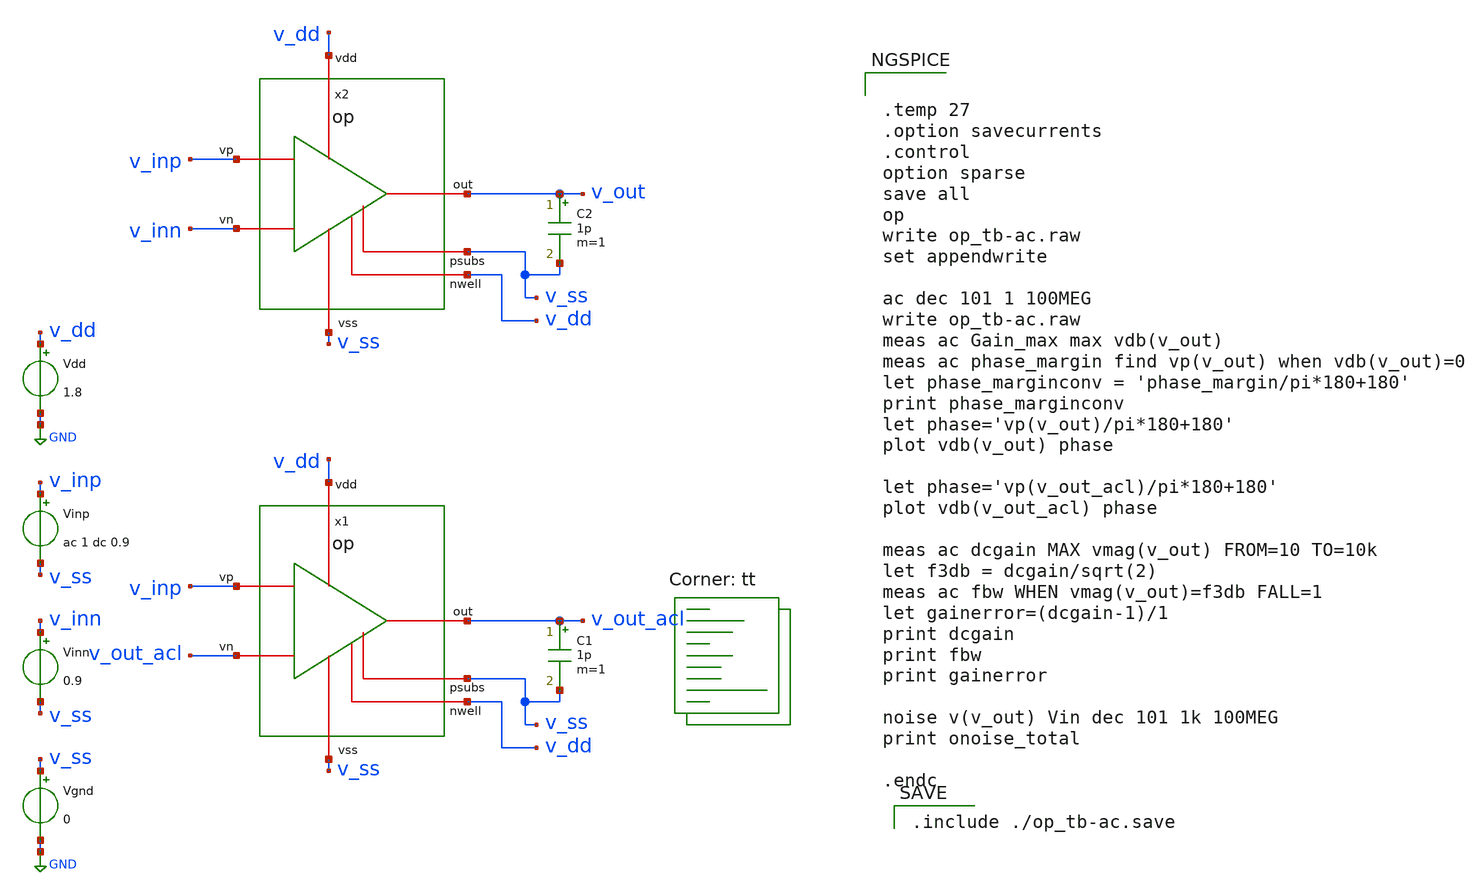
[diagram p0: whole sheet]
** sch_path: xschem/op_tb-ac.sch
**.subckt op_tb-ac
Vdd v_dd GND 1.8
Vinn v_inn v_ss 0.9
x1 v_out_acl v_dd v_ss v_inp v_out_acl v_ss v_dd op
Vgnd v_ss GND 0
C1 v_out_acl v_ss 1p m=1
Vinp v_inp v_ss ac 1 dc 0.9
x2 v_out v_dd v_ss v_inp v_inn v_ss v_dd op
C2 v_out v_ss 1p m=1
**** begin user architecture code
.lib $::SKYWATER_MODELS/sky130.lib.spice tt


.temp 27
.option savecurrents
.control
option sparse
save all
op
write op_tb-ac.raw
set appendwrite

ac dec 101 1 100MEG
write op_tb-ac.raw
meas ac Gain_max max vdb(v_out)
meas ac phase_margin find vp(v_out) when vdb(v_out)=0
let phase_marginconv = 'phase_margin/pi*180+180'
print phase_marginconv
let phase='vp(v_out)/pi*180+180'
plot vdb(v_out) phase

let phase='vp(v_out_acl)/pi*180+180'
plot vdb(v_out_acl) phase

meas ac dcgain MAX vmag(v_out) FROM=10 TO=10k
let f3db = dcgain/sqrt(2)
meas ac fbw WHEN vmag(v_out)=f3db FALL=1
let gainerror=(dcgain-1)/1
print dcgain
print fbw
print gainerror

noise v(v_out) Vin dec 101 1k 100MEG
print onoise_total

.endc


 .include ./op_tb-ac.save

**** end user architecture code
**.ends

* expanding   symbol:  op.sym # of pins=7
** sym_path: xschem/op.sym
** sch_path: xschem/op.sch
.subckt op out vdd vss vp vn psubs nwell
*.iopin vss
*.iopin vdd
*.opin out
*.ipin vp
*.ipin vn
*.iopin psubs
*.iopin nwell
XM3 out net1 vdd nwell sky130_fd_pr__pfet_01v8 L={l3} W={w3} nf={nf3} ad='int((nf+1)/2) * W/nf * 0.29'
+ as='int((nf+2)/2) * W/nf * 0.29' pd='2*int((nf+1)/2) * (W/nf + 0.29)' ps='2*int((nf+2)/2) * (W/nf + 0.29)'
+ nrd='0.29 / W' nrs='0.29 / W' sa=0 sb=0 sd=0 mult=1 m=1
XM1b net1 vn net2 psubs sky130_fd_pr__nfet_01v8 L={l1} W={w1} nf={nf1} ad='int((nf+1)/2) * W/nf * 0.29'
+ as='int((nf+2)/2) * W/nf * 0.29' pd='2*int((nf+1)/2) * (W/nf + 0.29)' ps='2*int((nf+2)/2) * (W/nf + 0.29)'
+ nrd='0.29 / W' nrs='0.29 / W' sa=0 sb=0 sd=0 mult=1 m=1
XM1a net3 vp net2 psubs sky130_fd_pr__nfet_01v8 L={l1} W={w1} nf={nf1} ad='int((nf+1)/2) * W/nf * 0.29'
+ as='int((nf+2)/2) * W/nf * 0.29' pd='2*int((nf+1)/2) * (W/nf + 0.29)' ps='2*int((nf+2)/2) * (W/nf + 0.29)'
+ nrd='0.29 / W' nrs='0.29 / W' sa=0 sb=0 sd=0 mult=1 m=1
XR1 net4 net1 vss sky130_fd_pr__res_high_po_0p35 L={lrz} mult=1 m=1
XC1 out net4 sky130_fd_pr__cap_mim_m3_1 W={wc} L={wc} MF={mc} m={mc}
**** begin user architecture code


.include ../sizing_opamp.spice


**** end user architecture code
XM2a net3 net3 vdd nwell sky130_fd_pr__pfet_01v8 L={l2} W={w2} nf={nf2} ad='int(({nf2} + 1)/2) * {w2} / {nf2} * 0.29'
+ as='int(({nf2} + 2)/2) * {w2} / {nf2} * 0.29' pd='2*int(({nf2} + 1)/2) * ({w2} / {nf2} + 0.29)' ps='2*int(({nf2} + 2)/2) * ({w2} / {nf2} + 0.29)'
+ nrd='0.29 / {w2} ' nrs='0.29 / {w2} ' sa=0 sb=0 sd=0 mult=1 m=1
XM2b net1 net3 vdd nwell sky130_fd_pr__pfet_01v8 L={l2} W={w2} nf={nf2} ad='int(({nf2} + 1)/2) * {w2} / {nf2} * 0.29'
+ as='int(({nf2} + 2)/2) * {w2} / {nf2} * 0.29' pd='2*int(({nf2} + 1)/2) * ({w2} / {nf2} + 0.29)' ps='2*int(({nf2} + 2)/2) * ({w2} / {nf2} + 0.29)'
+ nrd='0.29 / {w2} ' nrs='0.29 / {w2} ' sa=0 sb=0 sd=0 mult=1 m=1
XM0a bias bias vss psubs sky130_fd_pr__nfet_01v8 L={l0} W={w0} nf={nf0} ad='int(({nf0} + 1)/2) * {w0} / {nf0} * 0.29'
+ as='int(({nf0} + 2)/2) * {w0} / {nf0} * 0.29' pd='2*int(({nf0} + 1)/2) * ({w0} / {nf0} + 0.29)' ps='2*int(({nf0} + 2)/2) * ({w0} / {nf0} + 0.29)'
+ nrd='0.29 / {w0} ' nrs='0.29 / {w0} ' sa=0 sb=0 sd=0 mult=1 m=1
I0 vdd bias {i_tail}
XM0b net2 bias vss psubs sky130_fd_pr__nfet_01v8 L={l0} W={w0} nf={nf0} ad='int(({nf0} + 1)/2) * {w0} / {nf0} * 0.29'
+ as='int(({nf0} + 2)/2) * {w0} / {nf0} * 0.29' pd='2*int(({nf0} + 1)/2) * ({w0} / {nf0} + 0.29)' ps='2*int(({nf0} + 2)/2) * ({w0} / {nf0} + 0.29)'
+ nrd='0.29 / {w0} ' nrs='0.29 / {w0} ' sa=0 sb=0 sd=0 mult=1 m=1
XM0c out bias vss psubs sky130_fd_pr__nfet_01v8 L={l0} W={w0} nf={nf0} ad='int(({nf0} + 1)/2) * {w0} / {nf0} * 0.29'
+ as='int(({nf0} + 2)/2) * {w0} / {nf0} * 0.29' pd='2*int(({nf0} + 1)/2) * ({w0} / {nf0} + 0.29)' ps='2*int(({nf0} + 2)/2) * ({w0} / {nf0} + 0.29)'
+ nrd='0.29 / {w0} ' nrs='0.29 / {w0} ' sa=0 sb=0 sd=0 mult=1 m=1
.ends

.GLOBAL GND
.end
